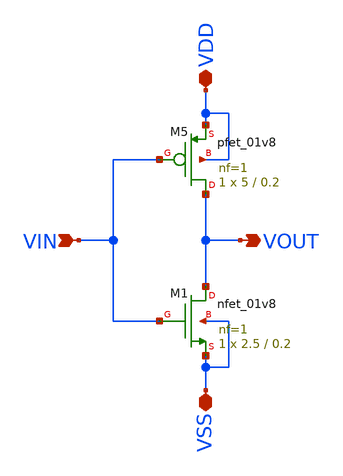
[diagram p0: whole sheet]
** sch_path: Xschem/PLL_TOP_Schematics/inverter.sch
* Copyright 2022 GlobalFoundries PDK Authors
* Licensed under the Apache License, Version 2.0 (the "License");
* you may not use this file except in compliance with the License.
* You may obtain a copy of the License at
* https://www.apache.org/licenses/LICENSE-2.0
* Unless required by applicable law or agreed to in writing, software
* distributed under the License is distributed on an "AS IS" BASIS,
* WITHOUT WARRANTIES OR CONDITIONS OF ANY KIND, either express or implied.
* See the License for the specific language governing permissions and
* limitations under the License.
**.subckt inverter VDD VIN VOUT VSS
*.iopin VDD
*.ipin VIN
*.opin VOUT
*.iopin VSS
XM5 VOUT VIN VDD VDD sky130_fd_pr__pfet_01v8 L=0.2 W=5 nf=1 ad='int((nf+1)/2) * W/nf * 0.29' as='int((nf+2)/2) * W/nf * 0.29'
+ pd='2*int((nf+1)/2) * (W/nf + 0.29)' ps='2*int((nf+2)/2) * (W/nf + 0.29)' nrd='0.29 / W' nrs='0.29 / W'
+ sa=0 sb=0 sd=0 mult=1 m=1
XM1 VOUT VIN VSS VSS sky130_fd_pr__nfet_01v8 L=0.2 W=2.5 nf=1 ad='int((nf+1)/2) * W/nf * 0.29' as='int((nf+2)/2) * W/nf * 0.29'
+ pd='2*int((nf+1)/2) * (W/nf + 0.29)' ps='2*int((nf+2)/2) * (W/nf + 0.29)' nrd='0.29 / W' nrs='0.29 / W'
+ sa=0 sb=0 sd=0 mult=1 m=1
**.ends
.end
